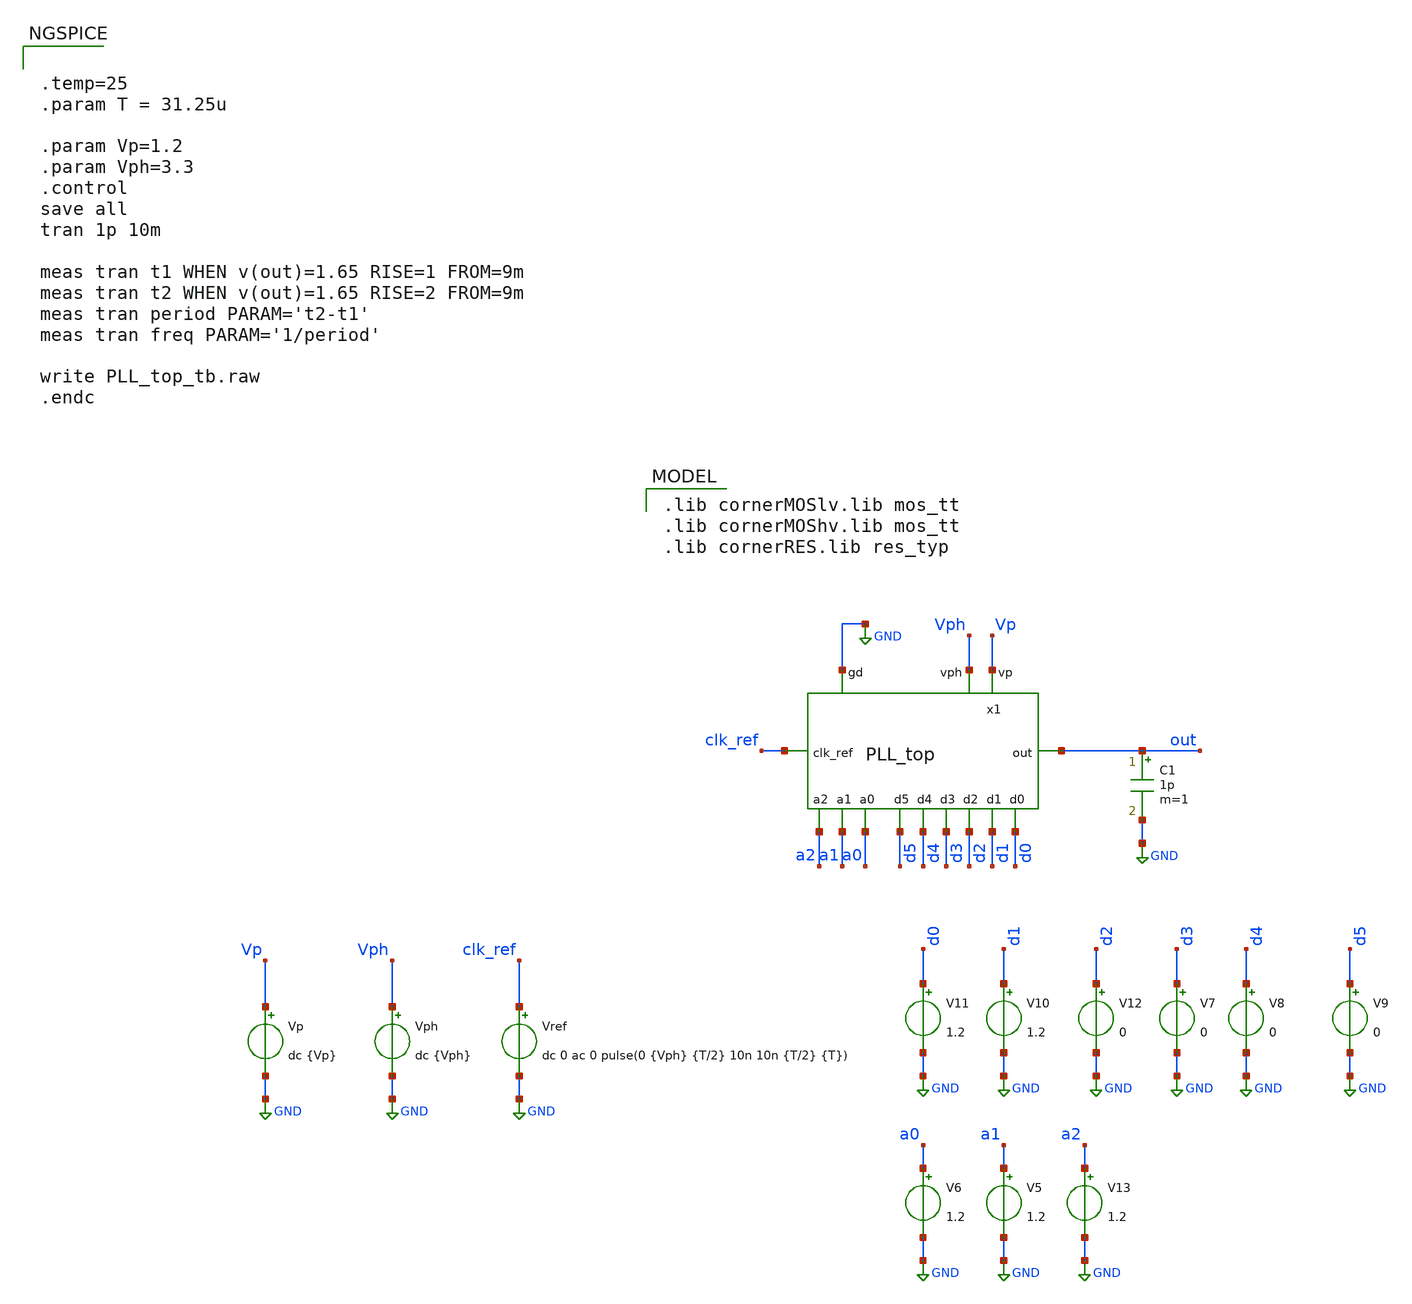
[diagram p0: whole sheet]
** sch_path: schematics/top/PLL_top_tb.sch
**.subckt PLL_top_tb
x1 Vp Vph GND clk_ref out d5 d3 a1 d2 d1 d0 d4 a2 a0 PLL_top
Vref clk_ref GND dc 0 ac 0 pulse(0 {Vph} {T/2} 10n 10n {T/2} {T})
Vp Vp GND dc {Vp}
Vph Vph GND dc {Vph}
C1 out GND 1p m=1
V8 d4 GND 0
V9 d5 GND 0
V11 d0 GND 1.2
V10 d1 GND 1.2
V12 d2 GND 0
V7 d3 GND 0
V5 a1 GND 1.2
V6 a0 GND 1.2
V13 a2 GND 1.2
**** begin user architecture code
 .lib cornerMOSlv.lib mos_tt
.lib cornerMOShv.lib mos_tt
.lib cornerRES.lib res_typ




.temp=25
.param T = 31.25u

.param Vp=1.2
.param Vph=3.3
.control
save all
tran 1p 10m

meas tran t1 WHEN v(out)=1.65 RISE=1 FROM=9m
meas tran t2 WHEN v(out)=1.65 RISE=2 FROM=9m
meas tran period PARAM='t2-t1'
meas tran freq PARAM='1/period'

write PLL_top_tb.raw
.endc


**** end user architecture code
**.ends
.GLOBAL GND
.end
